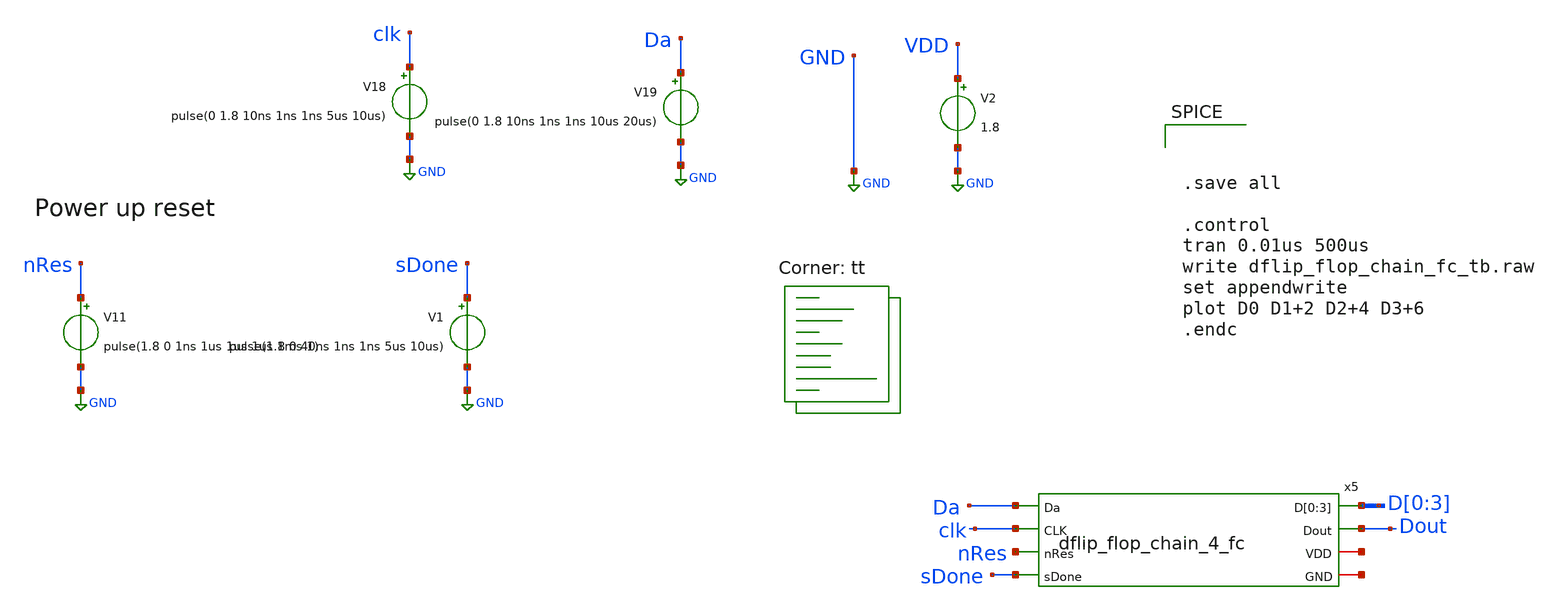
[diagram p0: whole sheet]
** sch_path: design/xschem/dflip_flop_chain_fc_tb.sch
**.subckt dflip_flop_chain_fc_tb
V2 VDD GND 1.8
V11 nRes GND pulse(1.8 0 1ns 1us 1us 1us 1ms 1)
V18 clk GND pulse(0 1.8 10ns 1ns 1ns 5us 10us)
V19 Da GND pulse(0 1.8 10ns 1ns 1ns 10us 20us)
V1 sDone GND pulse(1.8 0 40ns 1ns 1ns 5us 10us)
x5 Da D[0] D[1] D[2] D[3] Dout clk nRes sDone net1 net2 dflip_flop_chain_4_fc
**** begin user architecture code



.save all

.control
tran 0.01us 500us
write dflip_flop_chain_fc_tb.raw
set appendwrite
plot D0 D1+2 D2+4 D3+6
.endc




* Standard cell simulation files
.include $::SKYWATER_STDCELLS/sky130_fd_sc_hd.spice

* Power domains
VSTDCELL_PWR VPWR 0 DC 1.8
VSTDCELL_PB  VPB  0 DC 1.8
VSTDCELL_NB  VNB  0 DC 0
VSTDCELL_GND VGND 0 DC 0
.global VNB VGND VPB VPWR


.lib $::SKYWATER_MODELS/sky130.lib.spice tt
**** end user architecture code
**.ends

* expanding   symbol:  dflip_flop_chain_4_fc.sym # of pins=8
** sym_path: design/xschem/dflip_flop_chain_4_fc.sym
** sch_path: design/xschem/dflip_flop_chain_4_fc.sch
.subckt dflip_flop_chain_4_fc Da D[0] D[1] D[2] D[3] Dout CLK nRes sDone VDD GND
*.ipin Da
*.opin D[0],D[1],D[2],D[3]
*.ipin CLK
*.ipin nRes
*.ipin sDone
*.opin Dout
*.iopin VDD
*.iopin GND
x1[0] CLK Da nRes GND GND VDD VDD D_internal[0] sky130_fd_sc_hd__dfrtp_1
x1[1] CLK D_internal[0] nRes GND GND VDD VDD D_internal[1] sky130_fd_sc_hd__dfrtp_1
x1[2] CLK D_internal[1] nRes GND GND VDD VDD D_internal[2] sky130_fd_sc_hd__dfrtp_1
x1[3] CLK D_internal[2] nRes GND GND VDD VDD Dout sky130_fd_sc_hd__dfrtp_1
x2[0] D_internal[0] sDone nRes GND GND VDD VDD D[0] sky130_fd_sc_hd__dlrtp_1
x2[1] D_internal[1] sDone nRes GND GND VDD VDD D[1] sky130_fd_sc_hd__dlrtp_1
x2[2] D_internal[2] sDone nRes GND GND VDD VDD D[2] sky130_fd_sc_hd__dlrtp_1
x2[3] Dout sDone nRes GND GND VDD VDD D[3] sky130_fd_sc_hd__dlrtp_1
.ends

.GLOBAL GND
.end
